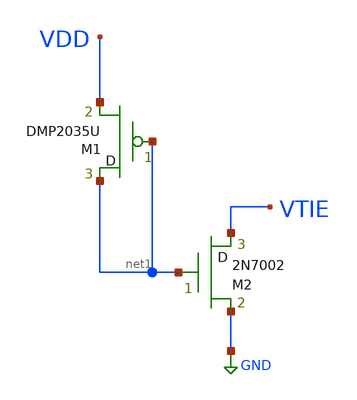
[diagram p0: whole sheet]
** sch_path: ISSCC25/accepted_notebooks/MicroNina/sch/DIGITAL_TIE_LOW.sch
**.subckt DIGITAL_TIE_LOW
M1 net1 net1 VDD DMP2035U m=1
M2 VTIE net1 GND M2N7002 m=1
**.ends
.GLOBAL GND
.end
